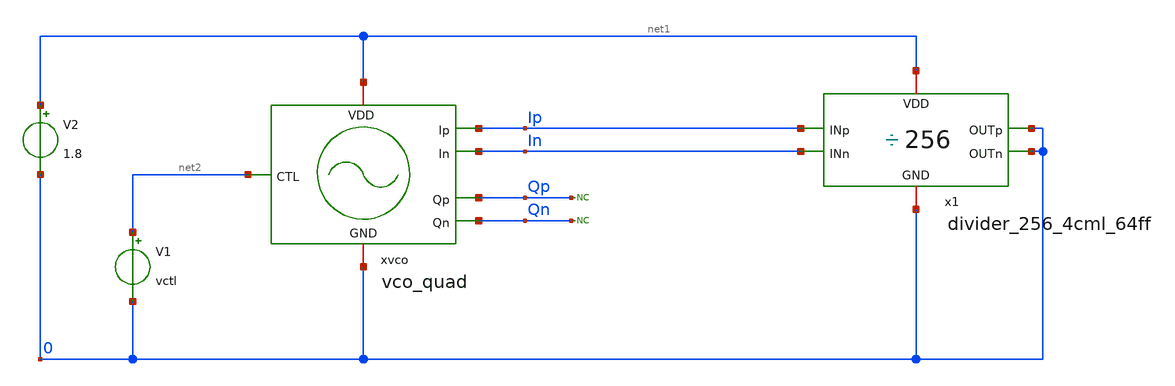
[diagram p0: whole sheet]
** sch_path: design/vco_quad/tests/vco_quad_tb.sch
**.subckt vco_quad_tb
xvco net1 net2 Ip In Qp Qn 0 vco_quad w_n=0.5u l_n=0.18u w_p= l_p=0.18u
V1 net2 0 vctl
V2 net1 0 1.8
x1 net1 0 Ip In 0 0 divider_256_4cml_64ff
* noconn Qp
* noconn Qn
**** begin user architecture code


.include '/home/tom/.xschem/simulations/xh018_ng/xh018.lib'
.temp 30
.param vctl=0.9
.tran  0.1e-9 1e-6 uic


**** end user architecture code
**.ends
.end
